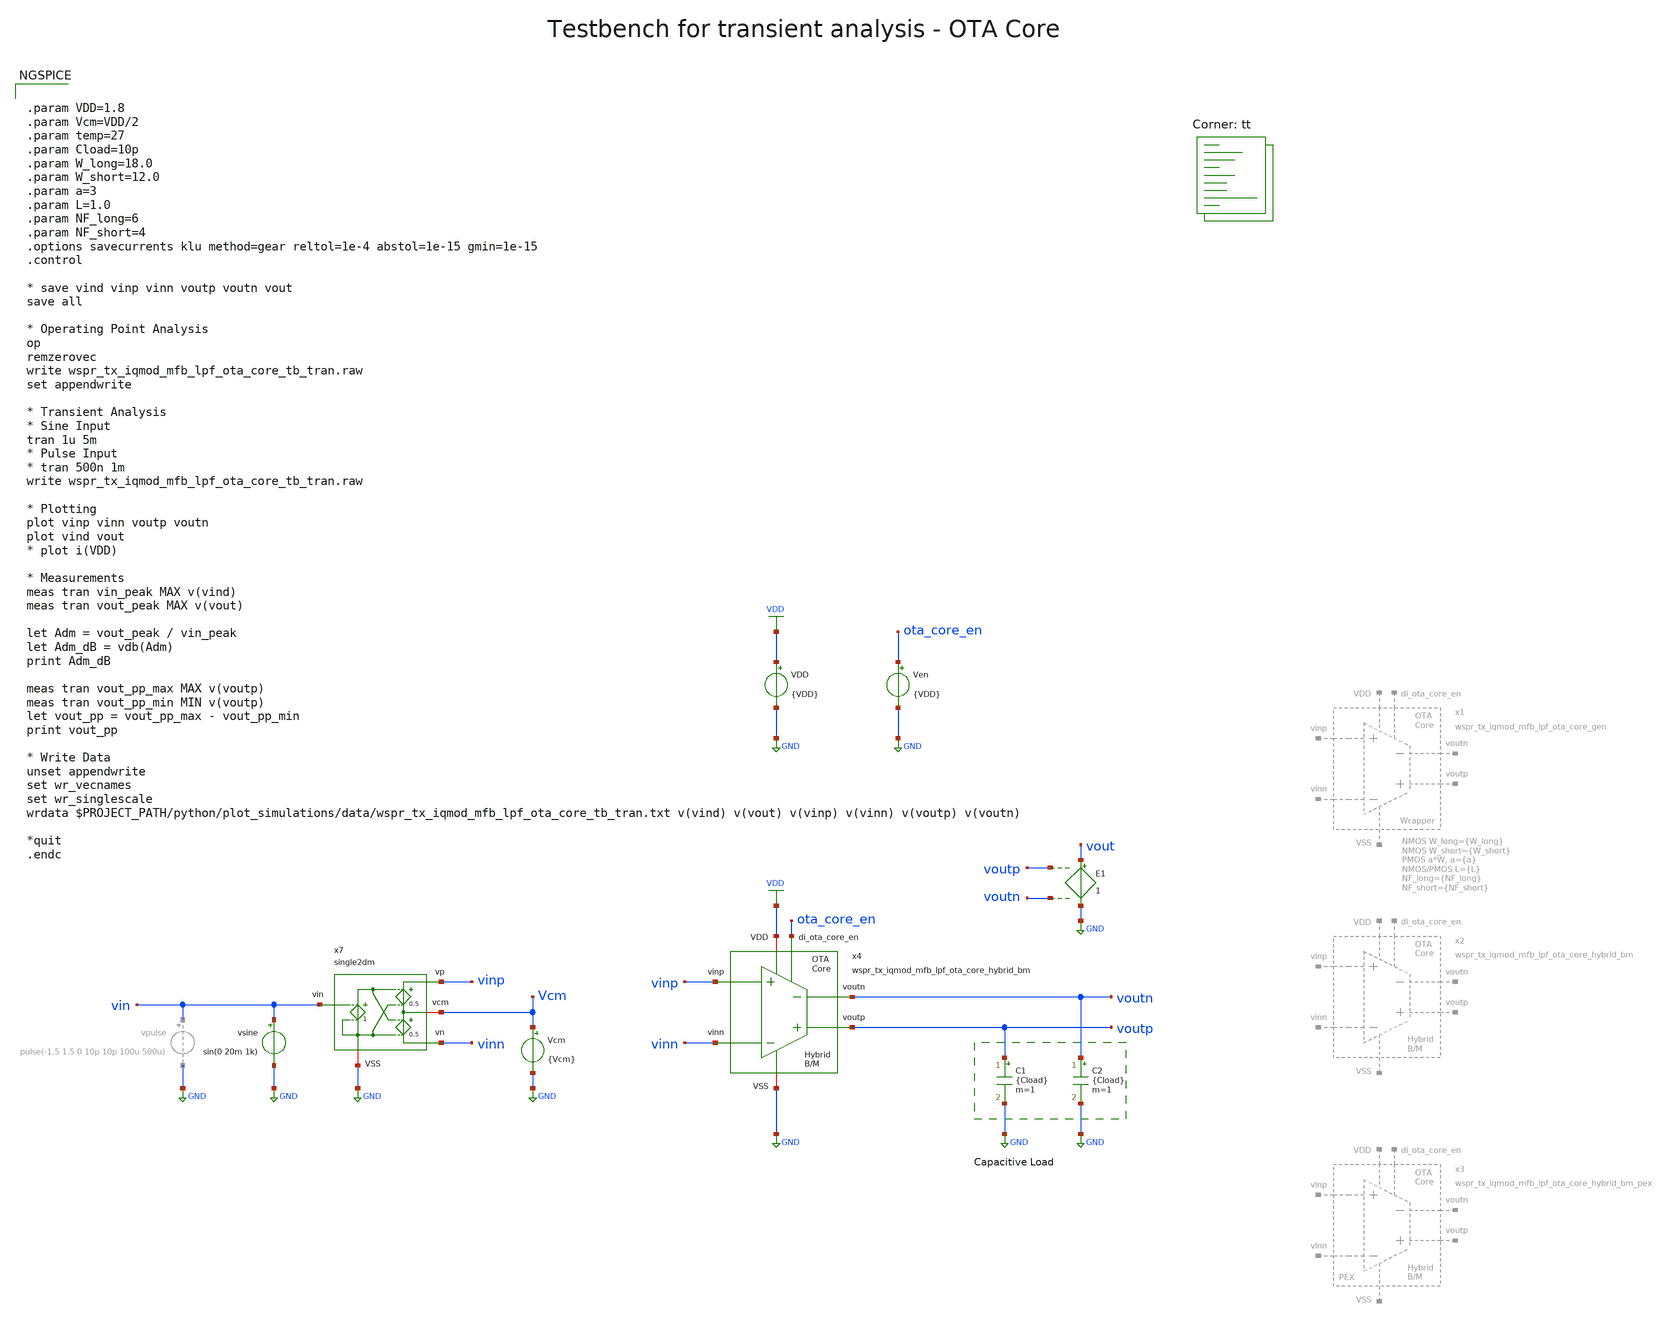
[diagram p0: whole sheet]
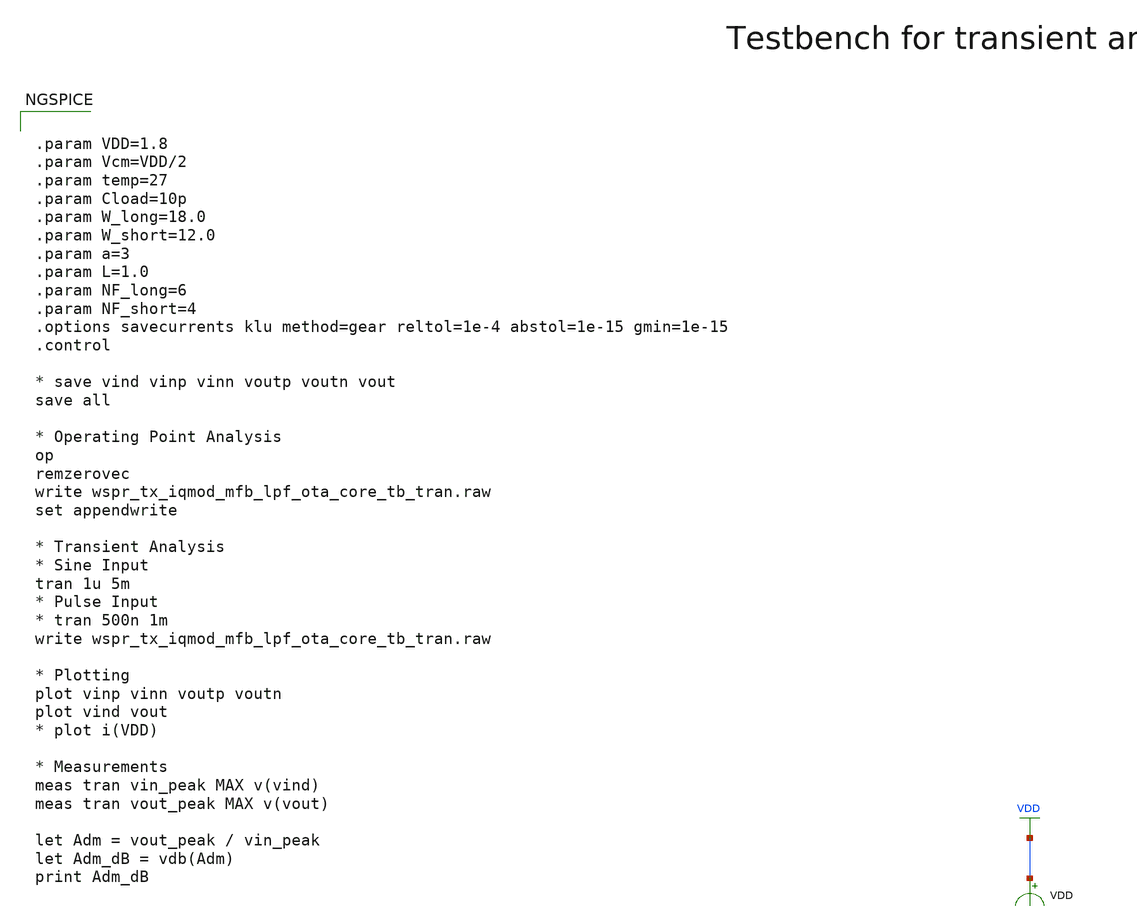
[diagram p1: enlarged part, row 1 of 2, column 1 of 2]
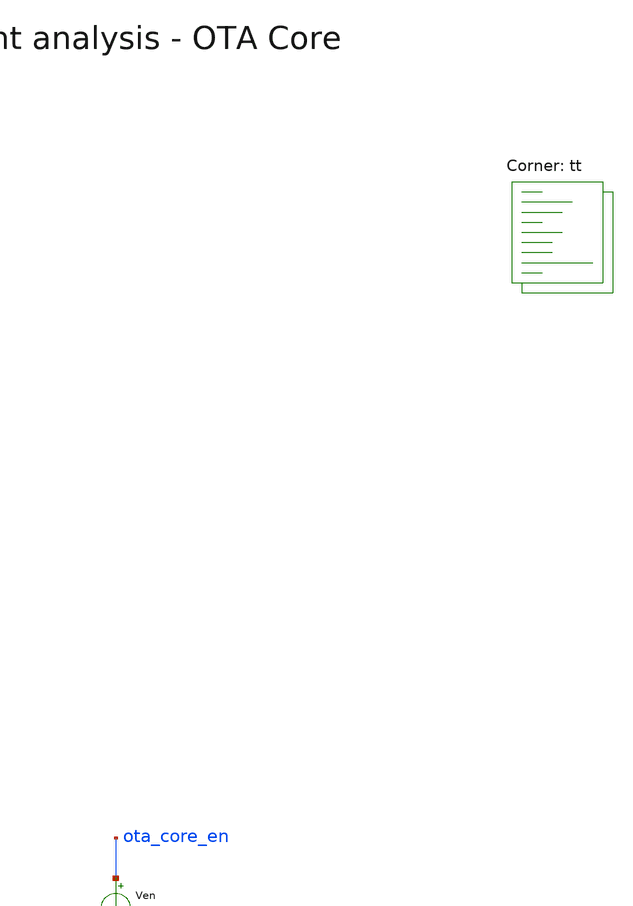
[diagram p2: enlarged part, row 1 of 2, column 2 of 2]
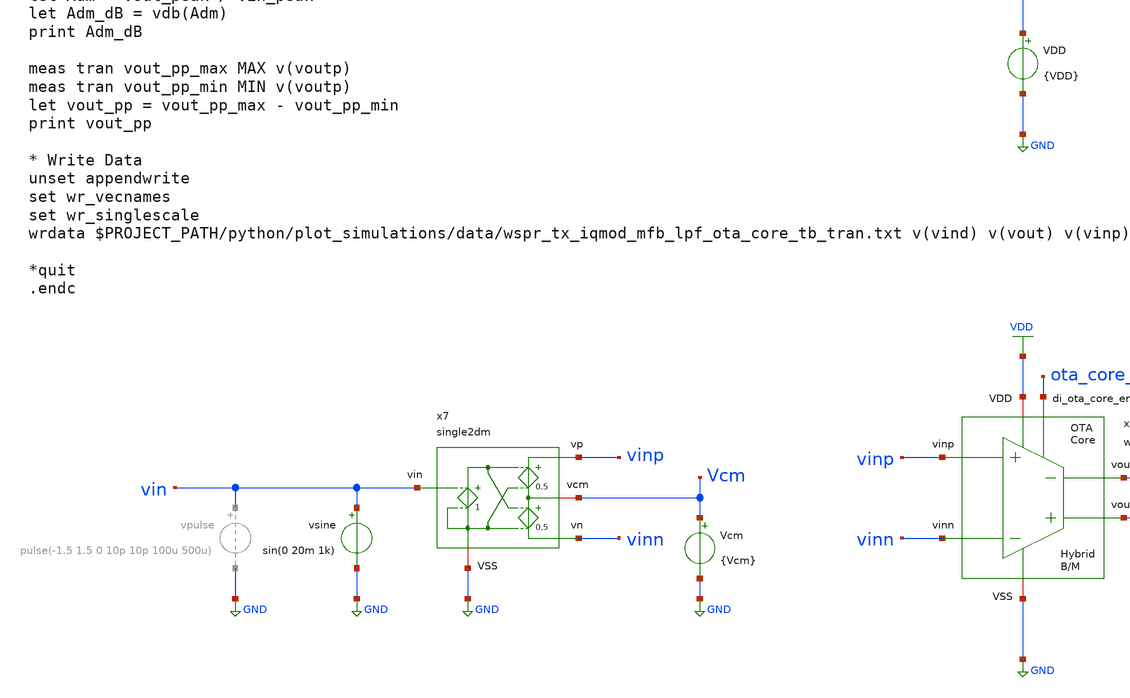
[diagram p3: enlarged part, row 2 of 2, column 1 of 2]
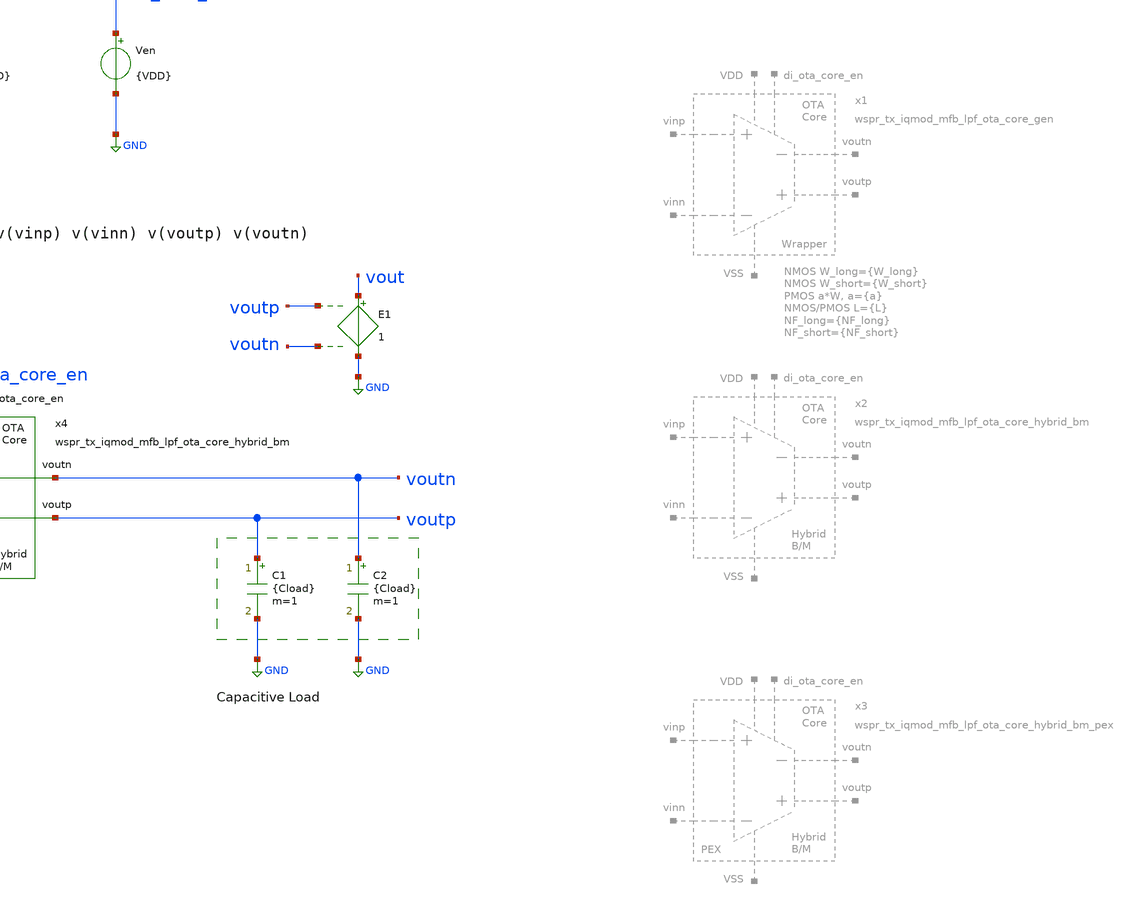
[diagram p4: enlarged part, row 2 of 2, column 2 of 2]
** sch_path: sky130/macros/iqmod/testbenches/wspr_tx_iqmod_mfb_lpf_ota_core_tb_tran.sch
**.subckt wspr_tx_iqmod_mfb_lpf_ota_core_tb_tran
VDD VDD GND {VDD}
C1 voutp GND {Cload} m=1
C2 voutn GND {Cload} m=1
E1 vout GND voutp voutn 1
Ven ota_core_en GND {VDD}
vsine vin GND sin(0 20m 1k)
Vcm Vcm GND {Vcm}
x7 vinp vin Vcm GND vinn single2dm
x4 ota_core_en voutp voutn vinn vinp VDD GND wspr_tx_iqmod_mfb_lpf_ota_core_hybrid_bm
**** begin user architecture code


.param VDD=1.8
.param Vcm=VDD/2
.param temp=27
.param Cload=10p
.param W_long=18.0
.param W_short=12.0
.param a=3
.param L=1.0
.param NF_long=6
.param NF_short=4
.options savecurrents klu method=gear reltol=1e-4 abstol=1e-15 gmin=1e-15
.control

* save vind vinp vinn voutp voutn vout
save all

* Operating Point Analysis
op
remzerovec
write wspr_tx_iqmod_mfb_lpf_ota_core_tb_tran.raw
set appendwrite

* Transient Analysis
* Sine Input
tran 1u 5m
* Pulse Input
* tran 500n 1m
write wspr_tx_iqmod_mfb_lpf_ota_core_tb_tran.raw

* Plotting
plot vinp vinn voutp voutn
plot vind vout
* plot i(VDD)

* Measurements
meas tran vin_peak MAX v(vind)
meas tran vout_peak MAX v(vout)

let Adm = vout_peak / vin_peak
let Adm_dB = vdb(Adm)
print Adm_dB

meas tran vout_pp_max MAX v(voutp)
meas tran vout_pp_min MIN v(voutp)
let vout_pp = vout_pp_max - vout_pp_min
print vout_pp

* Write Data
unset appendwrite
set wr_vecnames
set wr_singlescale
wrdata $PROJECT_PATH/python/plot_simulations/data/wspr_tx_iqmod_mfb_lpf_ota_core_tb_tran.txt v(vind)
+ v(vout) v(vinp) v(vinn) v(voutp) v(voutn)

*quit
.endc


.lib $::SKYWATER_MODELS/sky130.lib.spice tt
**** end user architecture code
**.ends
.GLOBAL GND
.GLOBAL VDD
.end
